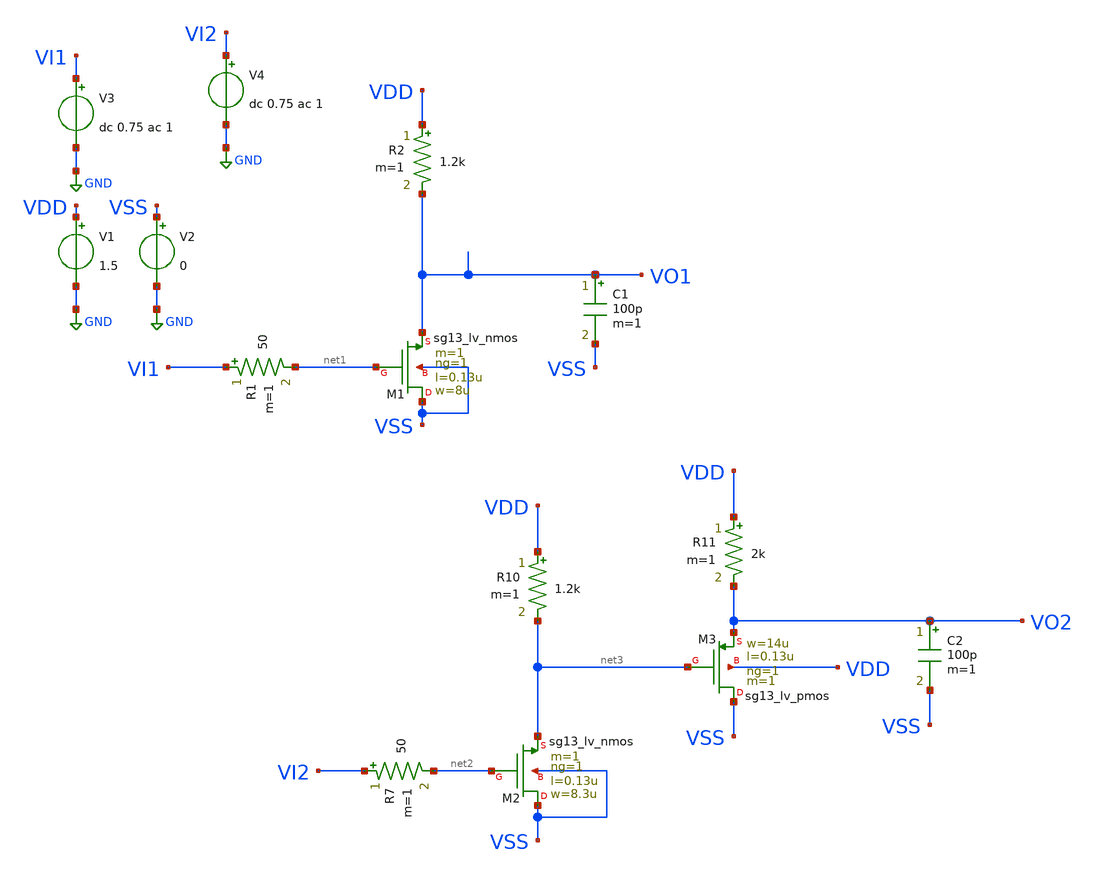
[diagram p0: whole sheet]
** sch_path: designs/1iee34/tb_nmos_amp.sch
**.subckt tb_nmos_amp
XM1 VSS net1 VO1 VSS sg13_lv_nmos w=8u l=0.13u ng=1 m=1 mm_ok=1
R1 VI1 net1 50 m=1
C1 VO1 VSS 100p m=1
R2 VDD VO1 1.2k m=1
V1 VDD GND 1.5
V2 VSS GND 0
V3 VI1 GND dc 0.75 ac 1
R7 VI2 net2 50 m=1
V4 VI2 GND dc 0.75 ac 1
XM2 VSS net2 net3 VSS sg13_lv_nmos w=8.3u l=0.13u ng=1 m=1 mm_ok=1
R10 VDD net3 1.2k m=1
R11 VDD VO2 2k m=1
XM3 VSS net3 VO2 VDD sg13_lv_pmos w=14u l=0.13u ng=1 m=1 mm_ok=1
C2 VO2 VSS 100p m=1
**** begin user architecture code

.lib cornerMOSlv.lib mos_tt



.param temp=27
.save all   @n.xm1.nsg13_lv_nmos[ids] @n.xm1.nsg13_lv_nmos[gm]  @n.xm2.nsg13_lv_nmos[ids] @n.xm2.nsg13_lv_nmos[gm]  @n.xm3.nsg13_lv_pmos[ids] @n.xm3.nsg13_lv_pmos[gm]

.control
  op
  set filetype = ascii
  write tb_nmos_amp.raw
.endc
.control
  ac dec 80 10k 10g
  set filetype = ascii
  set units=degrees
  write tb_nmos_amp.raw vdb(vo1) vp(vo1) vdb(vo2) vp(vo2)
  set appendwrite
  op
  set filetype = ascii
  write tb_nmos_amp.raw
.endc


**** end user architecture code
**.ends
.GLOBAL GND
.end
